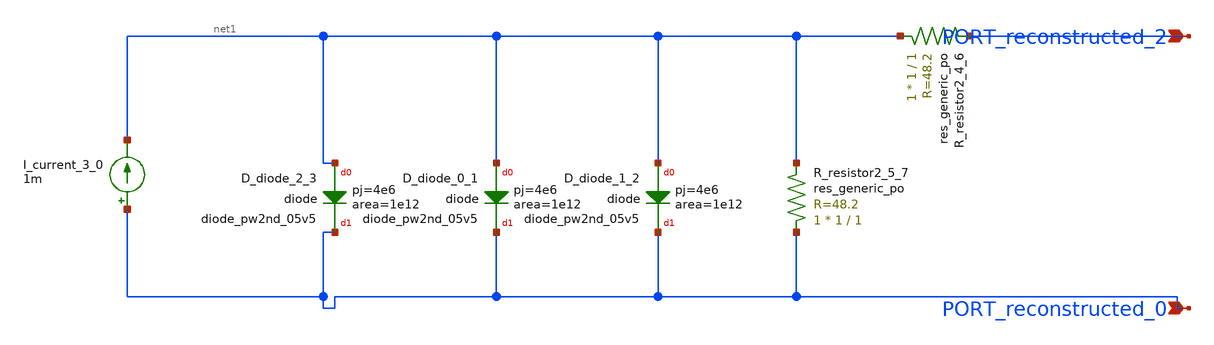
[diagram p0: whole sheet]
** sch_path: schematics/SchemGen/10_1109_ACCESS_2021_3052153_04_001.sch
**.subckt 10_1109_ACCESS_2021_3052153_04_001 PORT_reconstructed_0 PORT_reconstructed_2
*.ipin PORT_reconstructed_0
*.ipin PORT_reconstructed_2
I_current_3_0 PORT_reconstructed_0 net1 1m
XD_diode_0_1 net1 PORT_reconstructed_0 sky130_fd_pr__diode_pw2nd_05v5 area=1e12 pj=4e6
XD_diode_1_2 net1 PORT_reconstructed_0 sky130_fd_pr__diode_pw2nd_05v5 area=1e12 pj=4e6
XD_diode_2_3 net1 PORT_reconstructed_0 sky130_fd_pr__diode_pw2nd_05v5 area=1e12 pj=4e6
XR_resistor2_4_6 net1 PORT_reconstructed_2 sky130_fd_pr__res_generic_po W=1 L=1 m=1
XR_resistor2_5_7 PORT_reconstructed_0 net1 sky130_fd_pr__res_generic_po W=1 L=1 m=1
**.ends
.end
